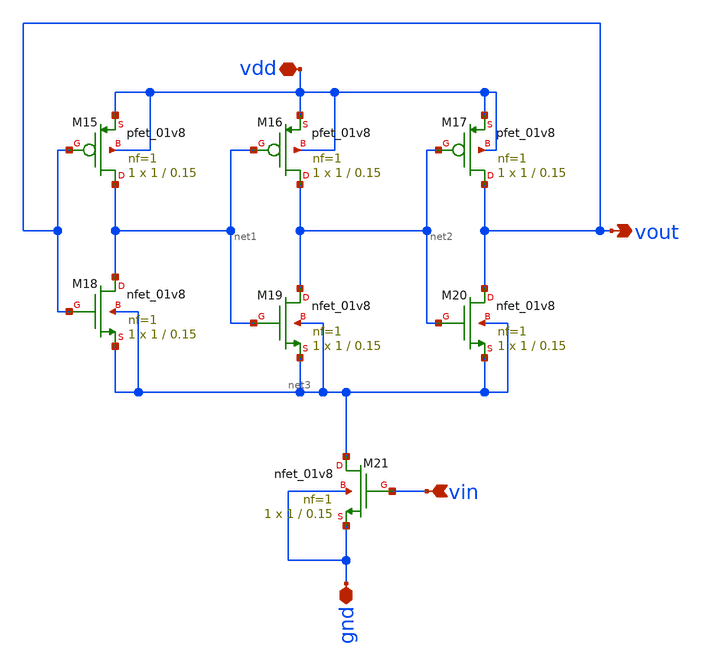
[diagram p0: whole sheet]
** sch_path: Neuron/voltContrOsc/sch/voltContrOsc.sch
**.subckt voltContrOsc gnd vdd vin vout
*.iopin gnd
*.iopin vdd
*.ipin vin
*.opin vout
XM15 net1 vout vdd vdd sky130_fd_pr__pfet_01v8 L=0.15 W=1 nf=1 ad='int((nf+1)/2) * W/nf * 0.29' as='int((nf+2)/2) * W/nf * 0.29'
+ pd='2*int((nf+1)/2) * (W/nf + 0.29)' ps='2*int((nf+2)/2) * (W/nf + 0.29)' nrd='0.29 / W' nrs='0.29 / W'
+ sa=0 sb=0 sd=0 mult=1 m=1
XM16 net2 net1 vdd vdd sky130_fd_pr__pfet_01v8 L=0.15 W=1 nf=1 ad='int((nf+1)/2) * W/nf * 0.29' as='int((nf+2)/2) * W/nf * 0.29'
+ pd='2*int((nf+1)/2) * (W/nf + 0.29)' ps='2*int((nf+2)/2) * (W/nf + 0.29)' nrd='0.29 / W' nrs='0.29 / W'
+ sa=0 sb=0 sd=0 mult=1 m=1
XM17 vout net2 vdd vdd sky130_fd_pr__pfet_01v8 L=0.15 W=1 nf=1 ad='int((nf+1)/2) * W/nf * 0.29' as='int((nf+2)/2) * W/nf * 0.29'
+ pd='2*int((nf+1)/2) * (W/nf + 0.29)' ps='2*int((nf+2)/2) * (W/nf + 0.29)' nrd='0.29 / W' nrs='0.29 / W'
+ sa=0 sb=0 sd=0 mult=1 m=1
XM18 net1 vout net3 net3 sky130_fd_pr__nfet_01v8 L=0.15 W=1 nf=1 ad='int((nf+1)/2) * W/nf * 0.29' as='int((nf+2)/2) * W/nf * 0.29'
+ pd='2*int((nf+1)/2) * (W/nf + 0.29)' ps='2*int((nf+2)/2) * (W/nf + 0.29)' nrd='0.29 / W' nrs='0.29 / W'
+ sa=0 sb=0 sd=0 mult=1 m=1
XM19 net2 net1 net3 net3 sky130_fd_pr__nfet_01v8 L=0.15 W=1 nf=1 ad='int((nf+1)/2) * W/nf * 0.29' as='int((nf+2)/2) * W/nf * 0.29'
+ pd='2*int((nf+1)/2) * (W/nf + 0.29)' ps='2*int((nf+2)/2) * (W/nf + 0.29)' nrd='0.29 / W' nrs='0.29 / W'
+ sa=0 sb=0 sd=0 mult=1 m=1
XM20 vout net2 net3 net3 sky130_fd_pr__nfet_01v8 L=0.15 W=1 nf=1 ad='int((nf+1)/2) * W/nf * 0.29' as='int((nf+2)/2) * W/nf * 0.29'
+ pd='2*int((nf+1)/2) * (W/nf + 0.29)' ps='2*int((nf+2)/2) * (W/nf + 0.29)' nrd='0.29 / W' nrs='0.29 / W'
+ sa=0 sb=0 sd=0 mult=1 m=1
XM21 net3 vin gnd gnd sky130_fd_pr__nfet_01v8 L=0.15 W=1 nf=1 ad='int((nf+1)/2) * W/nf * 0.29' as='int((nf+2)/2) * W/nf * 0.29'
+ pd='2*int((nf+1)/2) * (W/nf + 0.29)' ps='2*int((nf+2)/2) * (W/nf + 0.29)' nrd='0.29 / W' nrs='0.29 / W'
+ sa=0 sb=0 sd=0 mult=1 m=1
**.ends
.end
